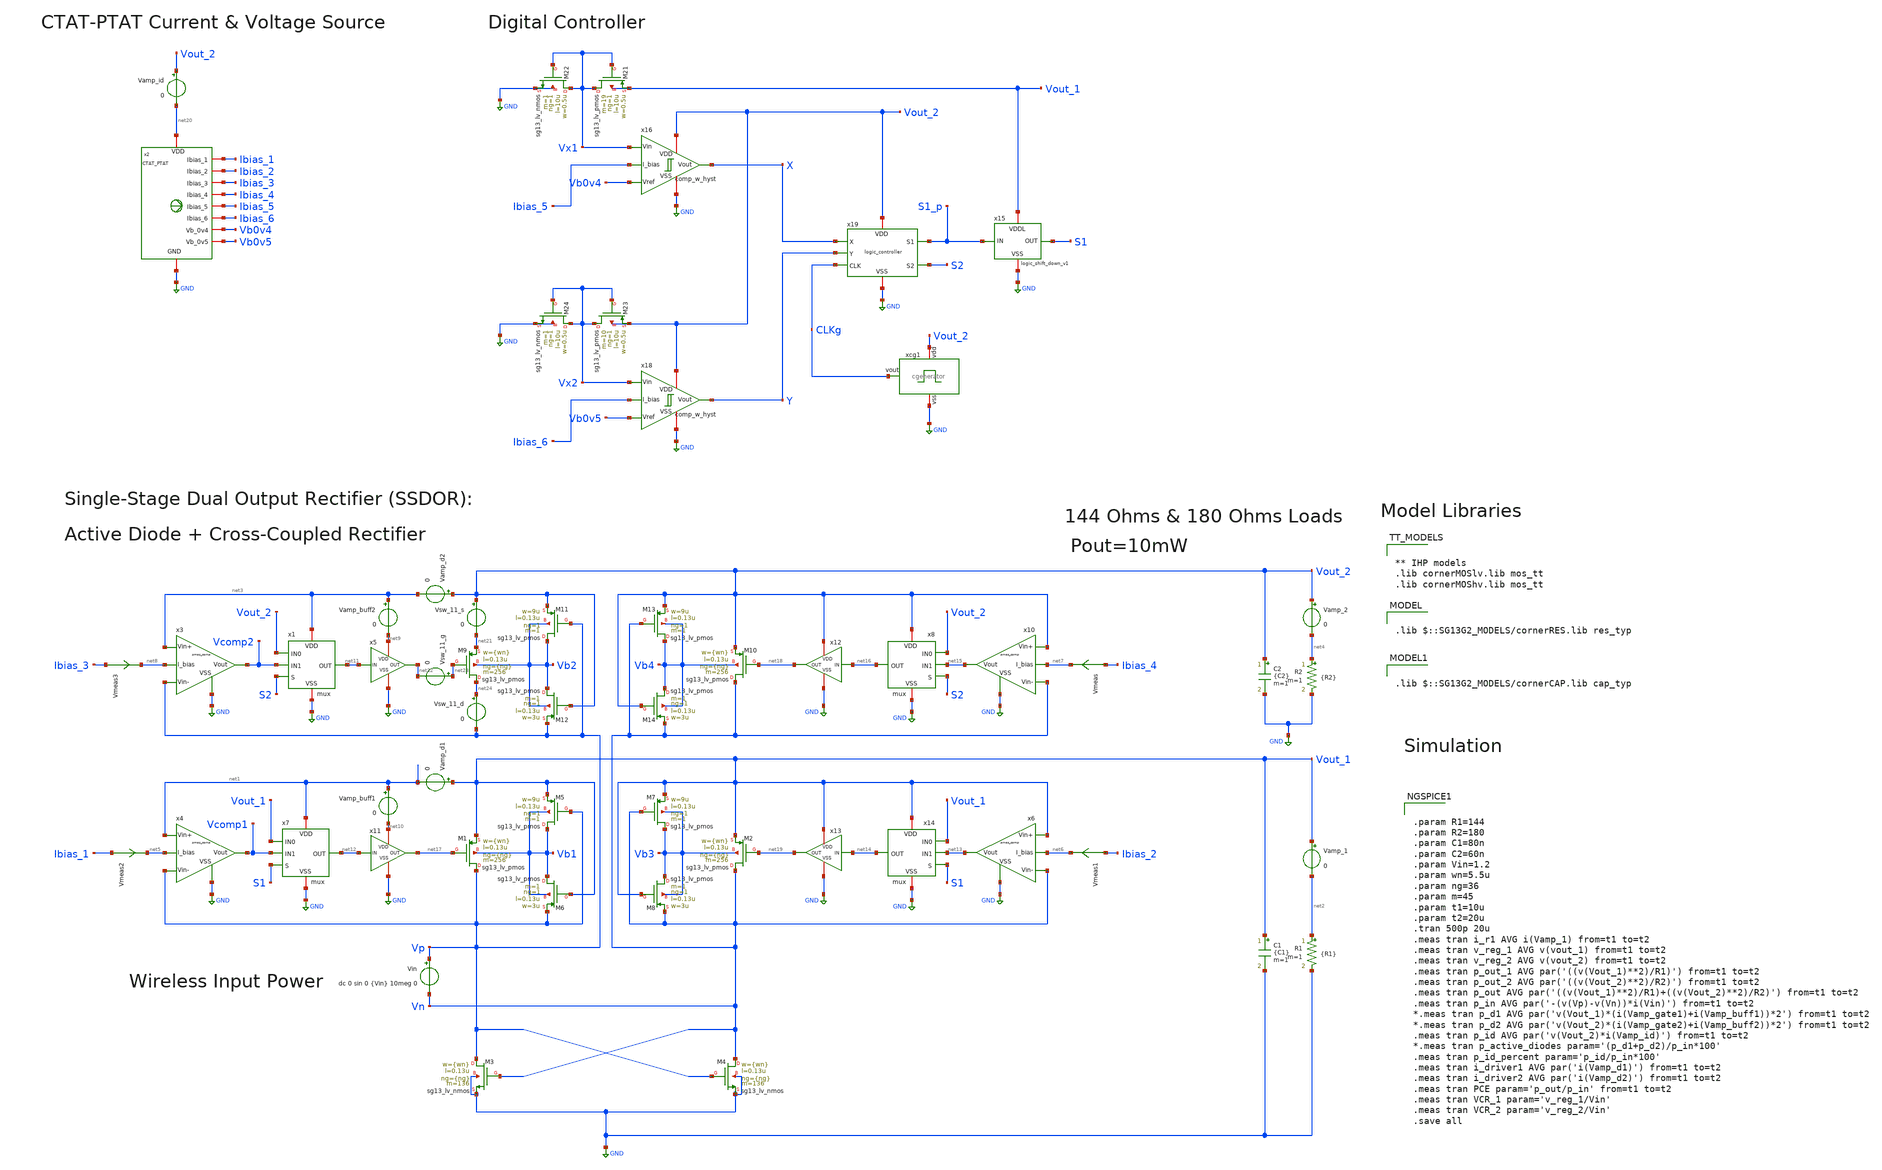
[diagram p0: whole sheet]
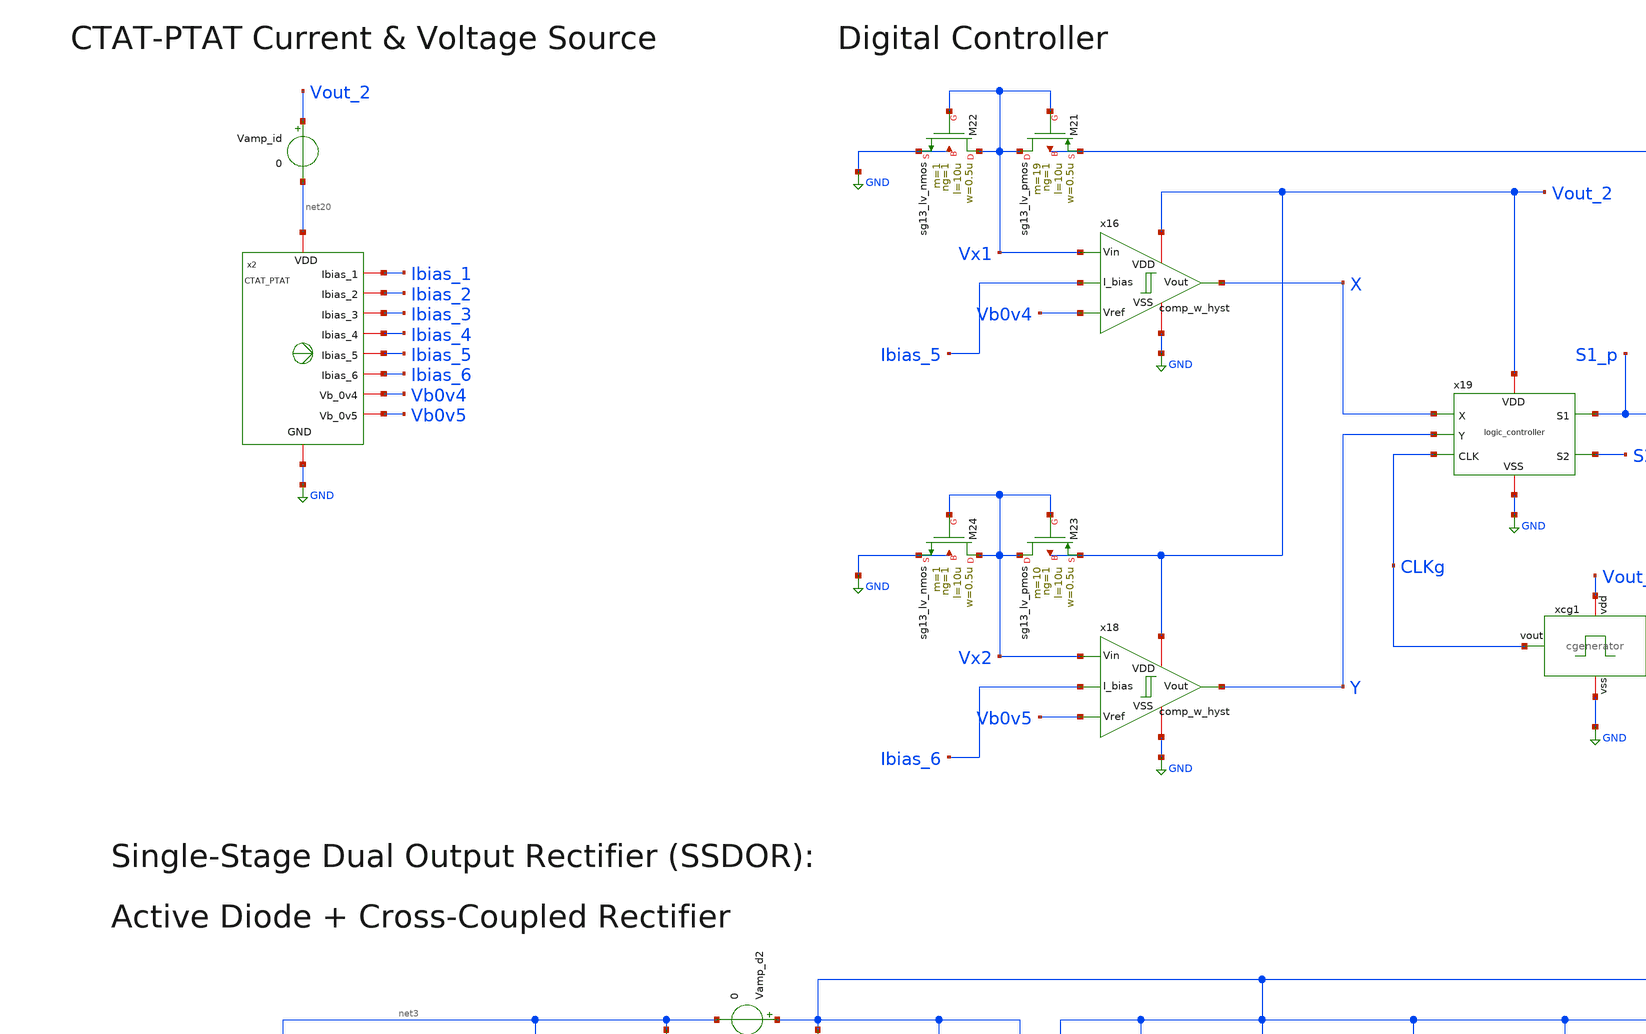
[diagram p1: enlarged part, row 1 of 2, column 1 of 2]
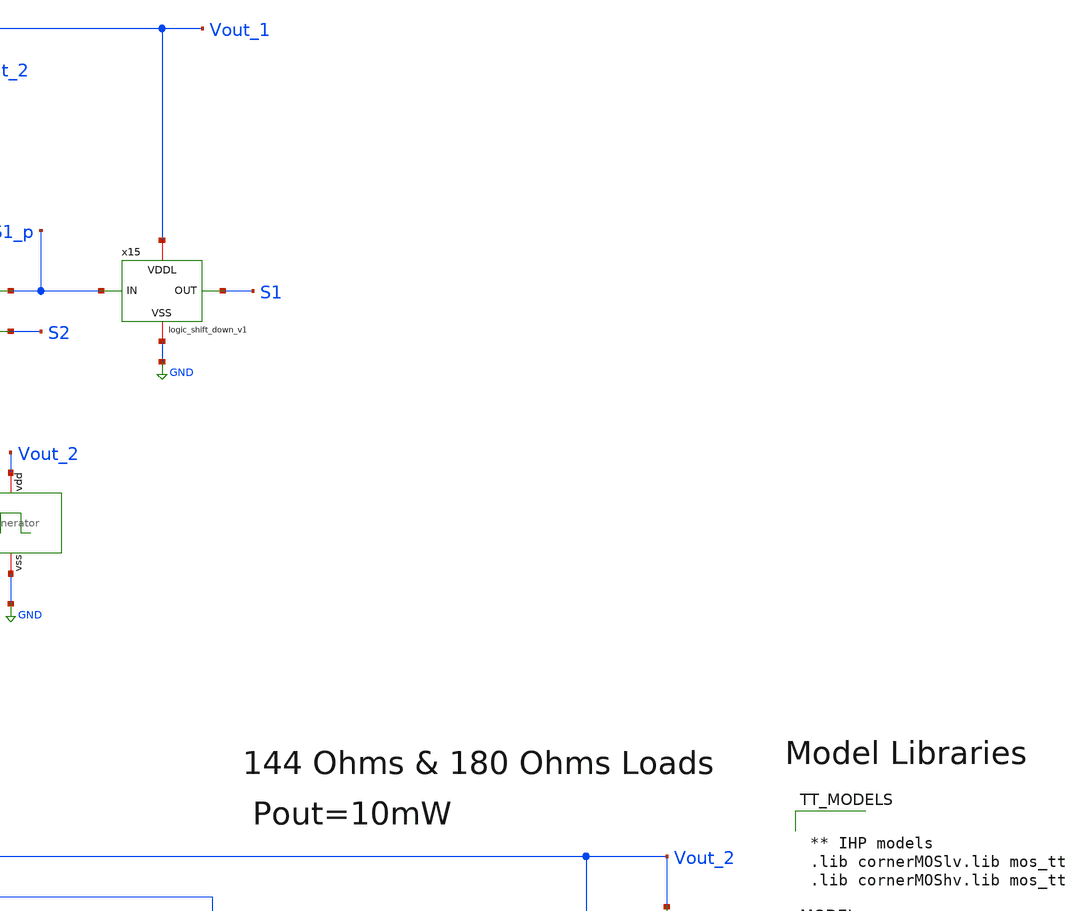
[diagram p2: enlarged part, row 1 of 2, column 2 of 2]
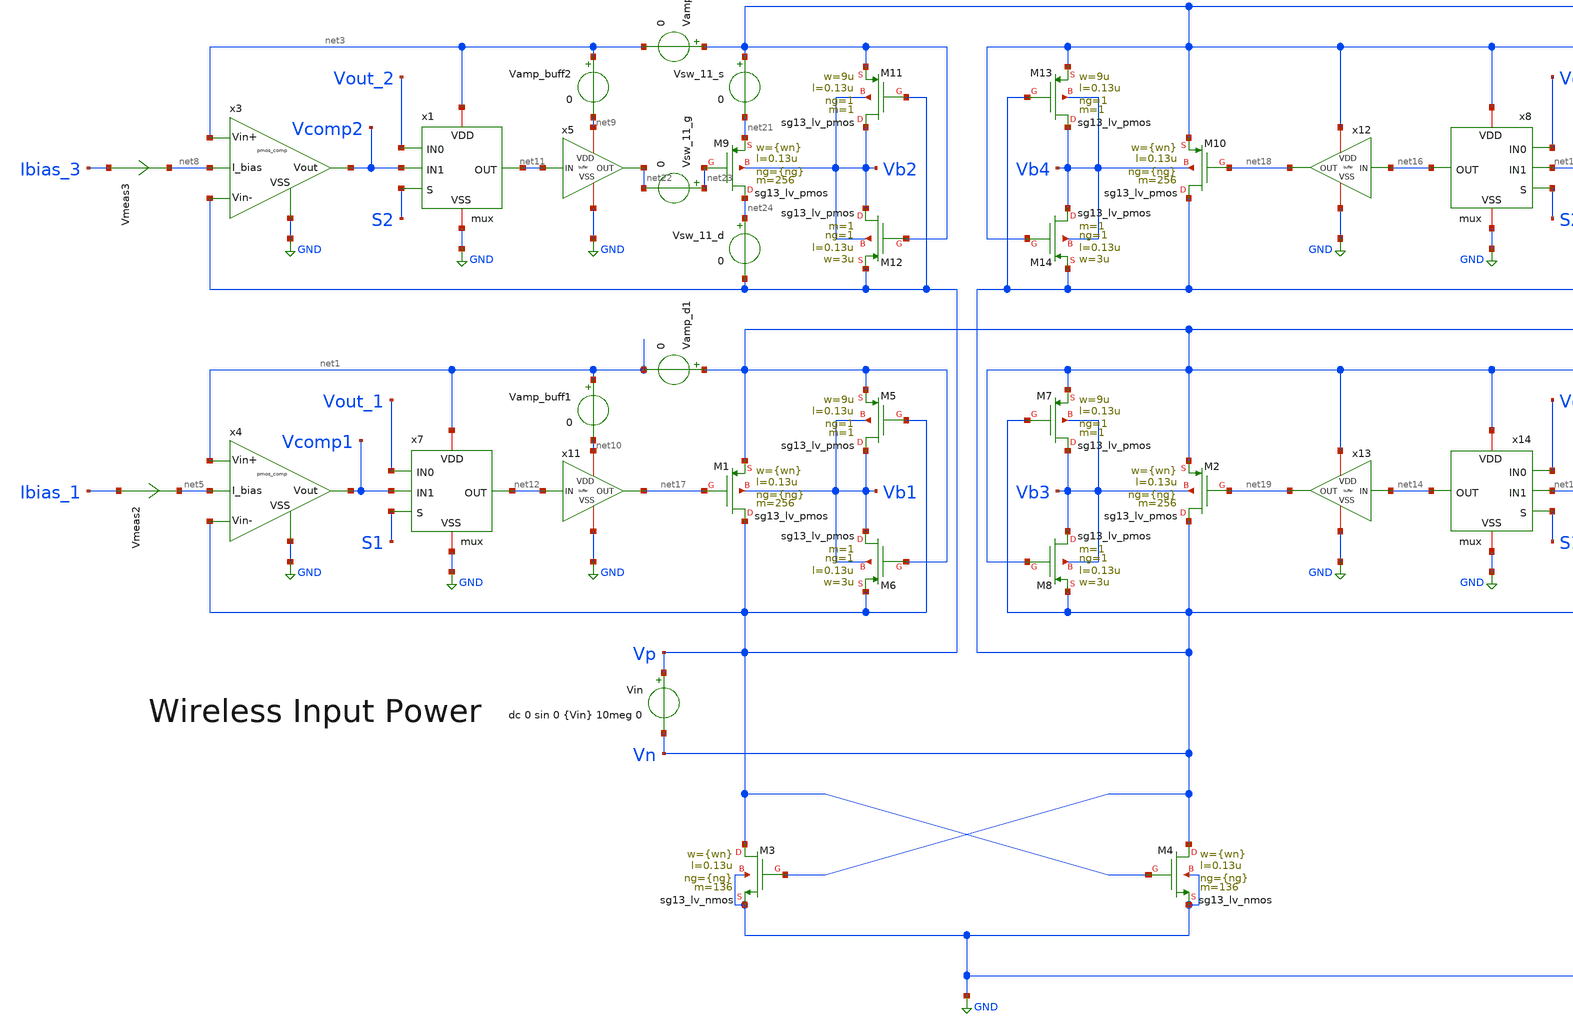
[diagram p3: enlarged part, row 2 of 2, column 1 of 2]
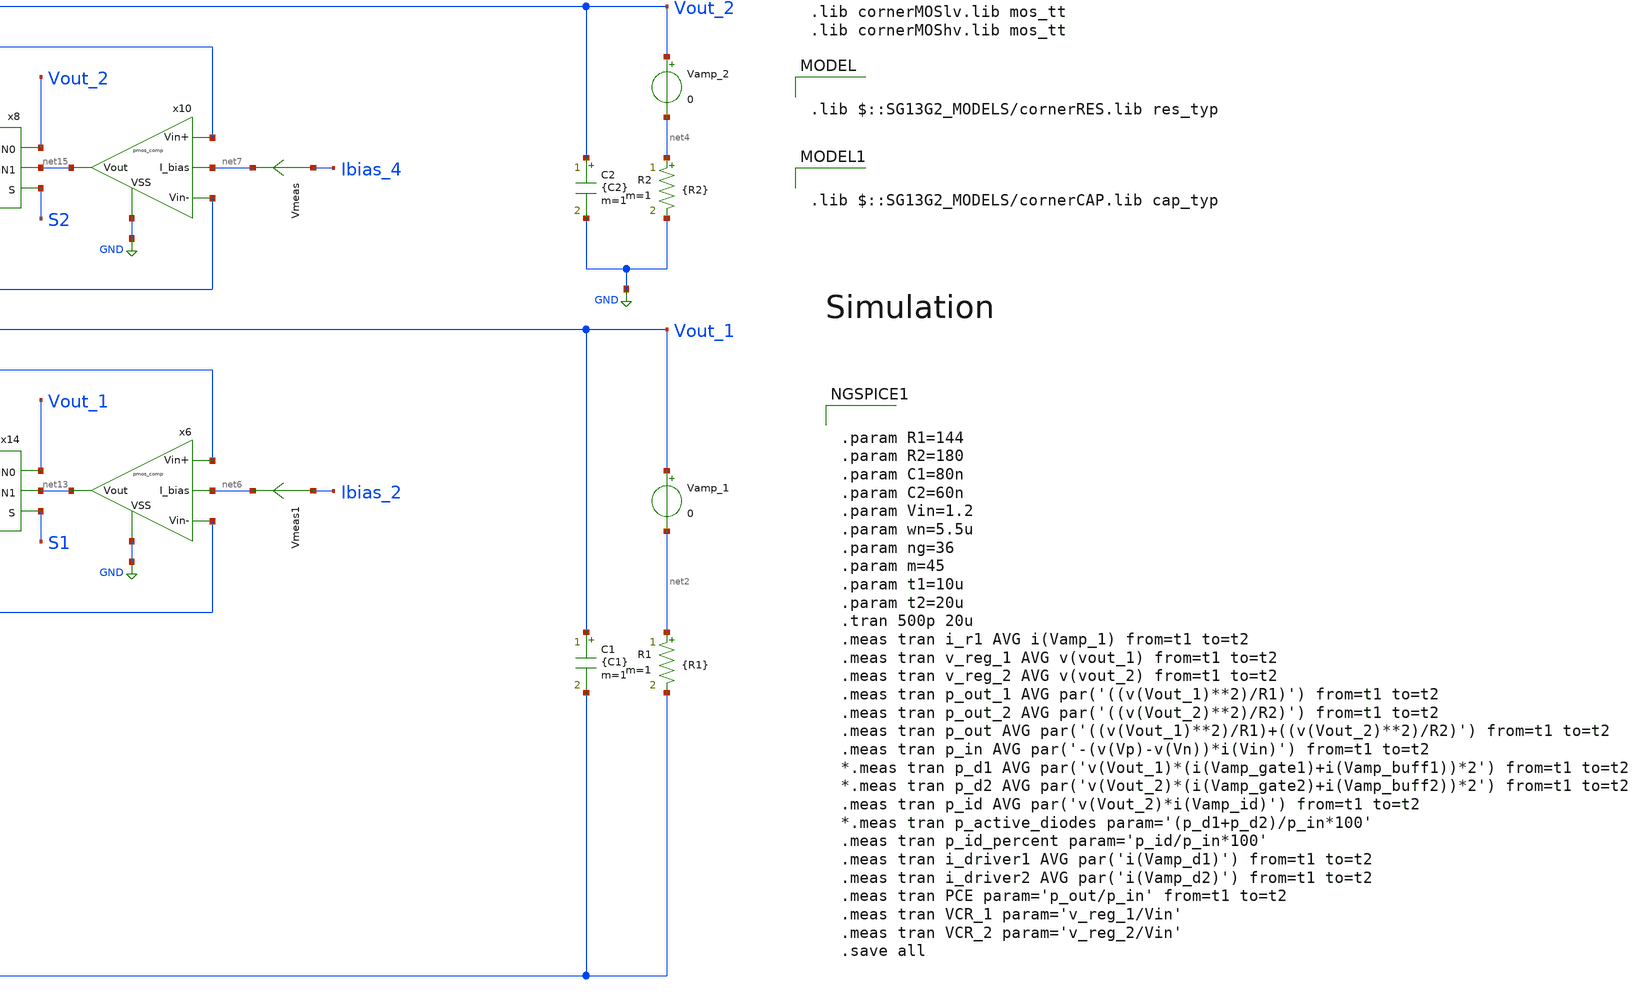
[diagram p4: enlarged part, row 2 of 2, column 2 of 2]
** sch_path: SSDOR_1.2V_v4/SSDOR_1.2V_v3.sch
**.subckt SSDOR_1.2V_v3
XM1 Vp net17 Vout_1 Vb1 sg13_lv_pmos w={wn} l=0.13u ng={ng} m=256 mm_ok=1
XM2 Vn net19 Vout_1 Vb3 sg13_lv_pmos w={wn} l=0.13u ng={ng} m=256 mm_ok=1
XM3 Vp Vn GND GND sg13_lv_nmos w={wn} l=0.13u ng={ng} m=136 mm_ok=1
XM4 Vn Vp GND GND sg13_lv_nmos w={wn} l=0.13u ng={ng} m=136 mm_ok=1
XM5 Vb1 Vp Vout_1 Vb1 sg13_lv_pmos w=9u l=0.13u ng=1 m=1 mm_ok=1
XM6 Vb1 Vout_1 Vp Vb1 sg13_lv_pmos w=3u l=0.13u ng=1 m=1 mm_ok=1
XM7 Vb3 Vn Vout_1 Vb3 sg13_lv_pmos w=9u l=0.13u ng=1 m=1 mm_ok=1
XM8 Vb3 Vout_1 Vn Vb3 sg13_lv_pmos w=3u l=0.13u ng=1 m=1 mm_ok=1
Vin Vp Vn dc 0 sin 0 {Vin} 10meg 0
C1 Vout_1 GND {C1} m=1
R1 net2 GND {R1} m=1
Vamp_1 Vout_1 net2 0
XM9 net24 net23 net21 Vb2 sg13_lv_pmos w={wn} l=0.13u ng={ng} m=256 mm_ok=1
XM10 Vn net18 Vout_2 Vb4 sg13_lv_pmos w={wn} l=0.13u ng={ng} m=256 mm_ok=1
XM11 Vb2 Vp Vout_2 Vb2 sg13_lv_pmos w=9u l=0.13u ng=1 m=1 mm_ok=1
XM12 Vb2 Vout_2 Vp Vb2 sg13_lv_pmos w=3u l=0.13u ng=1 m=1 mm_ok=1
XM13 Vb4 Vn Vout_2 Vb4 sg13_lv_pmos w=9u l=0.13u ng=1 m=1 mm_ok=1
XM14 Vb4 Vout_2 Vn Vb4 sg13_lv_pmos w=3u l=0.13u ng=1 m=1 mm_ok=1
C2 Vout_2 GND {C2} m=1
R2 net4 GND {R2} m=1
Vamp_2 Vout_2 net4 0
XM21 Vx1 Vx1 Vout_1 Vout_1 sg13_lv_pmos w=0.5u l=10u ng=1 m=19 mm_ok=1
XM22 Vx1 Vx1 GND GND sg13_lv_nmos w=0.5u l=10u ng=1 m=1 mm_ok=1
XM23 Vx2 Vx2 Vout_2 Vout_2 sg13_lv_pmos w=0.5u l=10u ng=1 m=10 mm_ok=1
XM24 Vx2 Vx2 GND GND sg13_lv_nmos w=0.5u l=10u ng=1 m=1 mm_ok=1
Vamp_d2 Vout_2 net3 0
Vamp_d1 Vout_1 net1 0
Vamp_buff2 net3 net9 0
Vamp_buff1 net1 net10 0
Vmeas Ibias_4 net7 0
.save i(vmeas)
Vmeas1 Ibias_2 net6 0
.save i(vmeas1)
Vmeas2 Ibias_1 net5 0
.save i(vmeas2)
Vmeas3 Ibias_3 net8 0
.save i(vmeas3)
Vamp_id Vout_2 net20 0
x2 net20 GND Ibias_4 Ibias_1 Ibias_2 Ibias_5 Ibias_6 Ibias_3 Vb0v5 Vb0v4 CTAT_PTAT
x16 Vout_2 GND Vb0v4 Vx1 X Ibias_5 comp_w_hyst
x18 Vout_2 GND Vb0v5 Vx2 Y Ibias_6 comp_w_hyst
x19 Vout_2 X S1_p CLKg Y S2 GND logic_controller
x15 Vout_1 S1_p S1 GND logic_shift_down_v1
x3 Vp net3 Vcomp2 net8 GND pmos_comp
x4 Vp net1 Vcomp1 net5 GND pmos_comp
x6 Vn Vout_1 net13 net6 GND pmos_comp
x10 Vn Vout_2 net15 net7 GND pmos_comp
x1 net3 Vout_2 S2 net11 Vcomp2 GND mux
x7 net1 Vout_1 S1 net12 Vcomp1 GND mux
x8 Vout_2 Vout_2 S2 net16 net15 GND mux
x14 Vout_1 Vout_1 S1 net14 net13 GND mux
x5 net9 net11 net22 GND buffer wn=1u
x11 net10 net12 net17 GND buffer wn=1u
x12 Vout_2 net16 net18 GND buffer wn=1u
x13 Vout_1 net14 net19 GND buffer wn=1u
xcg1 Vout_2 CLKg GND cgenerator
Vsw_11_s Vout_2 net21 0
Vsw_11_g net23 net22 0
Vsw_11_d net24 Vp 0
**** begin user architecture code


** IHP models
.lib cornerMOSlv.lib mos_tt
.lib cornerMOShv.lib mos_tt



.lib $::SG13G2_MODELS/cornerRES.lib res_typ


.lib $::SG13G2_MODELS/cornerCAP.lib cap_typ



.param R1=144
.param R2=180
.param C1=80n
.param C2=60n
.param Vin=1.2
.param wn=5.5u
.param ng=36
.param m=45
.param t1=10u
.param t2=20u
.tran 500p 20u
.meas tran i_r1 AVG i(Vamp_1) from=t1 to=t2
.meas tran v_reg_1 AVG v(vout_1) from=t1 to=t2
.meas tran v_reg_2 AVG v(vout_2) from=t1 to=t2
.meas tran p_out_1 AVG par('((v(Vout_1)**2)/R1)') from=t1 to=t2
.meas tran p_out_2 AVG par('((v(Vout_2)**2)/R2)') from=t1 to=t2
.meas tran p_out AVG par('((v(Vout_1)**2)/R1)+((v(Vout_2)**2)/R2)') from=t1 to=t2
.meas tran p_in AVG par('-(v(Vp)-v(Vn))*i(Vin)') from=t1 to=t2
*.meas tran p_d1 AVG par('v(Vout_1)*(i(Vamp_gate1)+i(Vamp_buff1))*2') from=t1 to=t2
*.meas tran p_d2 AVG par('v(Vout_2)*(i(Vamp_gate2)+i(Vamp_buff2))*2') from=t1 to=t2
.meas tran p_id AVG par('v(Vout_2)*i(Vamp_id)') from=t1 to=t2
*.meas tran p_active_diodes param='(p_d1+p_d2)/p_in*100'
.meas tran p_id_percent param='p_id/p_in*100'
.meas tran i_driver1 AVG par('i(Vamp_d1)') from=t1 to=t2
.meas tran i_driver2 AVG par('i(Vamp_d2)') from=t1 to=t2
.meas tran PCE param='p_out/p_in' from=t1 to=t2
.meas tran VCR_1 param='v_reg_1/Vin'
.meas tran VCR_2 param='v_reg_2/Vin'
.save all


**** end user architecture code
**.ends
.GLOBAL GND
.end
